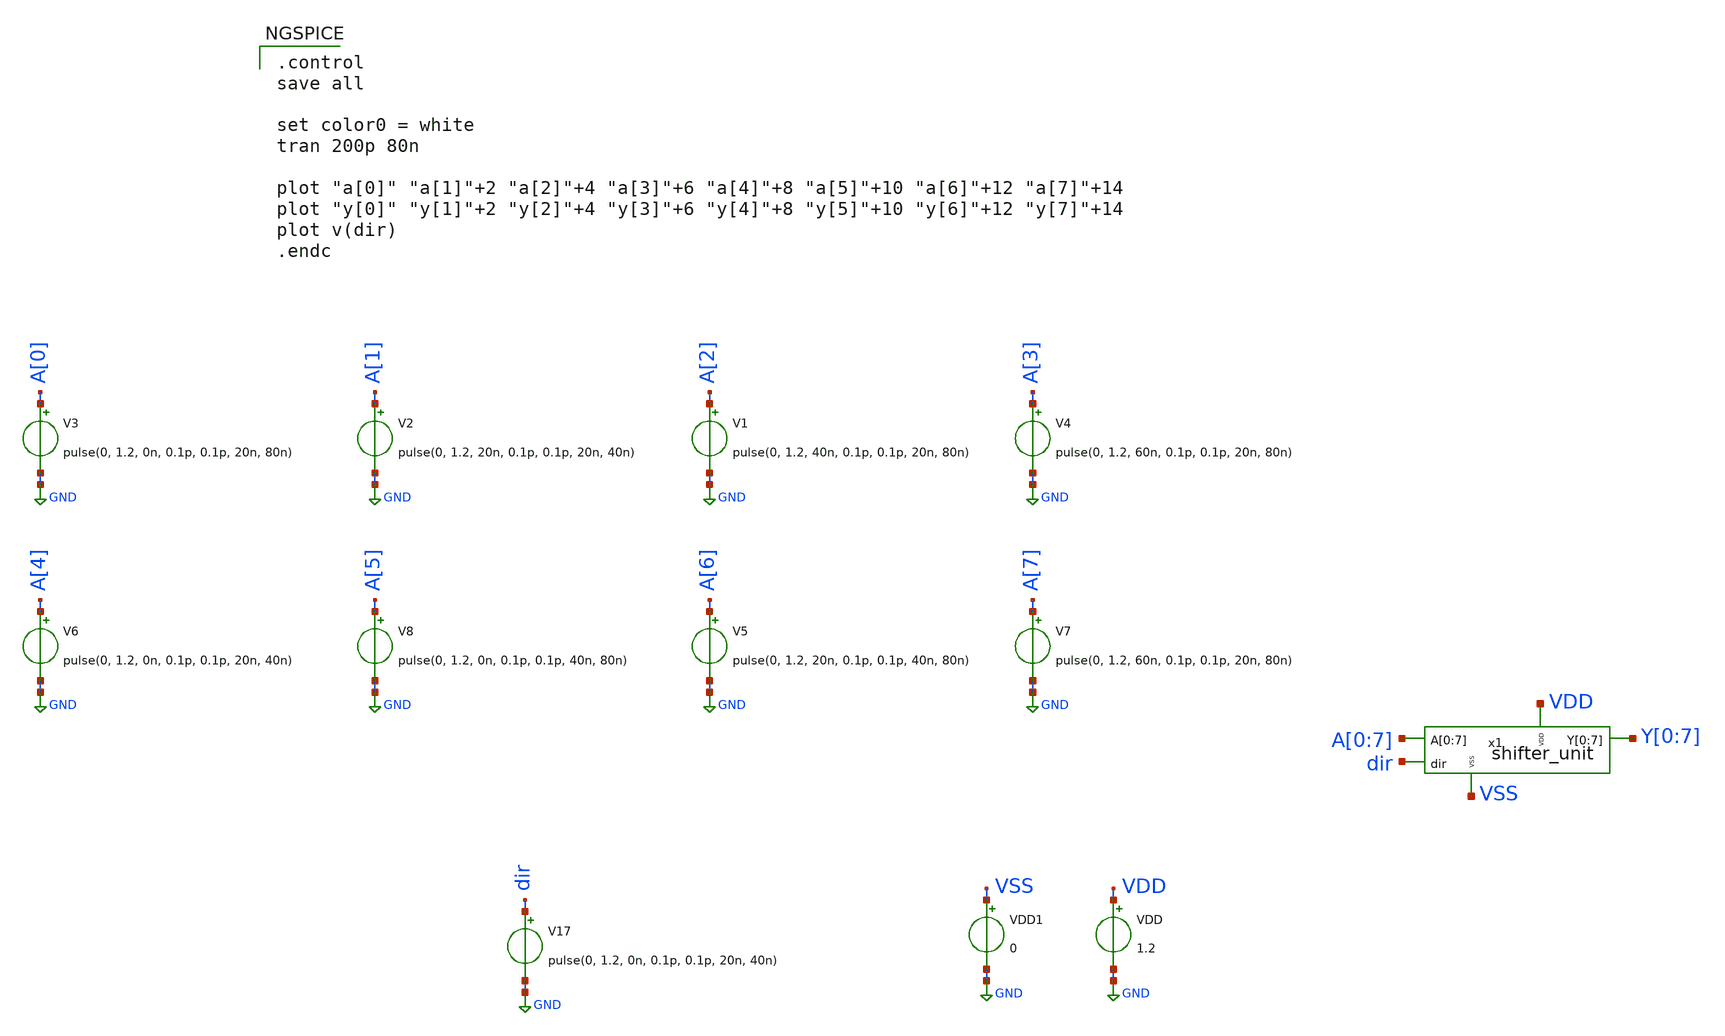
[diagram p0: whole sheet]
** sch_path: design/SHIFTER_UNIT/xschem/shifter_unit_tb.sch
**.subckt shifter_unit_tb
V17 dir GND pulse(0, 1.2, 0n, 0.1p, 0.1p, 20n, 40n)
V1 A[2] GND pulse(0, 1.2, 40n, 0.1p, 0.1p, 20n, 80n)
V3 A[0] GND pulse(0, 1.2, 0n, 0.1p, 0.1p, 20n, 80n)
V4 A[3] GND pulse(0, 1.2, 60n, 0.1p, 0.1p, 20n, 80n)
V2 A[1] GND pulse(0, 1.2, 20n, 0.1p, 0.1p, 20n, 40n)
V5 A[6] GND pulse(0, 1.2, 20n, 0.1p, 0.1p, 40n, 80n)
V6 A[4] GND pulse(0, 1.2, 0n, 0.1p, 0.1p, 20n, 40n)
V7 A[7] GND pulse(0, 1.2, 60n, 0.1p, 0.1p, 20n, 80n)
V8 A[5] GND pulse(0, 1.2, 0n, 0.1p, 0.1p, 40n, 80n)
VDD VDD GND 1.2
VDD1 VSS GND 0
x1 A[0] A[1] A[2] A[3] A[4] A[5] A[6] A[7] Y[0] Y[1] Y[2] Y[3] Y[4] Y[5] Y[6] Y[7] dir VSS VDD
+ shifter_unit
**** begin user architecture code

.control
save all

set color0 = white
tran 200p 80n

plot "a[0]" "a[1]"+2 "a[2]"+4 "a[3]"+6 "a[4]"+8 "a[5]"+10 "a[6]"+12 "a[7]"+14
plot "y[0]" "y[1]"+2 "y[2]"+4 "y[3]"+6 "y[4]"+8 "y[5]"+10 "y[6]"+12 "y[7]"+14
plot v(dir)
.endc


** opencircuitdesign pdks install
.lib $::SKYWATER_MODELS/sky130.lib.spice tt_mm


**** end user architecture code
**.ends

* expanding   symbol:  shifter_unit.sym # of pins=5
** sym_path: design/SHIFTER_UNIT/xschem/shifter_unit.sym
** sch_path: design/SHIFTER_UNIT/xschem/shifter_unit.sch
.subckt shifter_unit A[0] A[1] A[2] A[3] A[4] A[5] A[6] A[7] Y[0] Y[1] Y[2] Y[3] Y[4] Y[5] Y[6] Y[7]
+ dir VSS VDD
*.ipin A[0],A[1],A[2],A[3],A[4],A[5],A[6],A[7]
*.opin Y[0],Y[1],Y[2],Y[3],Y[4],Y[5],Y[6],Y[7]
*.ipin dir
*.iopin VSS
*.iopin VDD
x9 VSS VDD dir VSS A[1] Y[0] 2x1_mux
x1 VSS VDD dir A[0] A[2] Y[1] 2x1_mux
x2 VSS VDD dir A[1] A[3] Y[2] 2x1_mux
x3 VSS VDD dir A[2] A[4] Y[3] 2x1_mux
x4 VSS VDD dir A[3] A[5] Y[4] 2x1_mux
x5 VSS VDD dir A[4] A[6] Y[5] 2x1_mux
x6 VSS VDD dir A[5] A[7] Y[6] 2x1_mux
x7 VSS VDD dir A[6] VSS Y[7] 2x1_mux
.ends

.GLOBAL GND
.end
